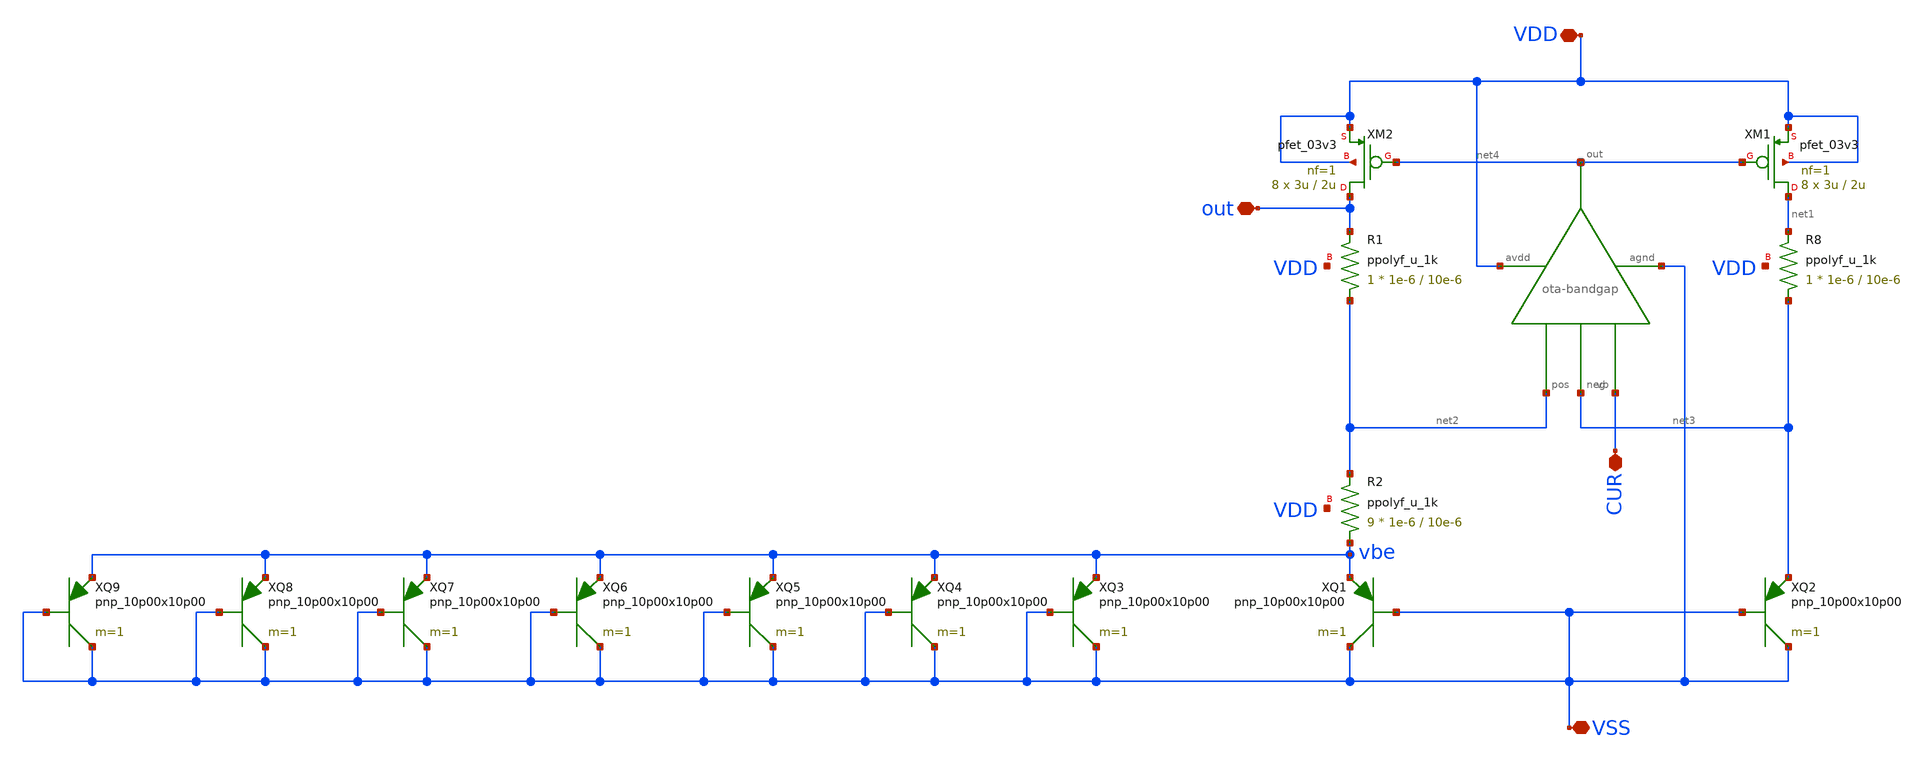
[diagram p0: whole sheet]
** sch_path: LDO/xschem/bandgap/bandgap.sch

.include $env(PDK_ROOT)/$env(PDK)/libs.tech/ngspice/design.ngspice
.lib $env(PDK_ROOT)/$env(PDK)/libs.tech/ngspice/sm141064.ngspice typical
.lib $env(PDK_ROOT)/$env(PDK)/libs.tech/ngspice/sm141064.ngspice mimcap_statistical
.lib $env(PDK_ROOT)/$env(PDK)/libs.tech/ngspice/sm141064.ngspice cap_mim
.lib $env(PDK_ROOT)/$env(PDK)/libs.tech/ngspice/sm141064.ngspice res_typical
.lib $env(PDK_ROOT)/$env(PDK)/libs.tech/ngspice/sm141064.ngspice bjt_typical
.lib $env(PDK_ROOT)/$env(PDK)/libs.tech/ngspice/sm141064.ngspice moscap_typical

**.subckt bandgap VDD VSS out CUR
*.iopin VDD
*.iopin VSS
*.iopin out
*.iopin CUR
XM1 net1 net4 VDD VDD pfet_03v3 L=2u W=3u nf=1 ad='int((nf+1)/2) * W/nf * 0.18u' as='int((nf+2)/2) * W/nf * 0.18u'
+ pd='2*int((nf+1)/2) * (W/nf + 0.18u)' ps='2*int((nf+2)/2) * (W/nf + 0.18u)' nrd='0.18u / W' nrs='0.18u / W'
+ sa=0 sb=0 sd=0 m=8
XM2 out net4 VDD VDD pfet_03v3 L=2u W=3u nf=1 ad='int((nf+1)/2) * W/nf * 0.18u' as='int((nf+2)/2) * W/nf * 0.18u'
+ pd='2*int((nf+1)/2) * (W/nf + 0.18u)' ps='2*int((nf+2)/2) * (W/nf + 0.18u)' nrd='0.18u / W' nrs='0.18u / W'
+ sa=0 sb=0 sd=0 m=8
X1 net4 VSS VDD net2 net3 CUR ota-bandgap
XQ1 VSS VSS vbe pnp_10p00x10p00 m=1
XQ2 VSS VSS net3 pnp_10p00x10p00 m=1
XQ3 VSS VSS vbe pnp_10p00x10p00 m=1
XQ4 VSS VSS vbe pnp_10p00x10p00 m=1
XQ5 VSS VSS vbe pnp_10p00x10p00 m=1
XQ6 VSS VSS vbe pnp_10p00x10p00 m=1
XQ7 VSS VSS vbe pnp_10p00x10p00 m=1
XQ8 VSS VSS vbe pnp_10p00x10p00 m=1
XQ9 VSS VSS vbe pnp_10p00x10p00 m=1
XR8 net3 net1 VDD ppolyf_u_1k r_width=1e-6 r_length=10e-6 m=1
XR1 net2 out VDD ppolyf_u_1k r_width=1e-6 r_length=10e-6 m=1
XR2 vbe net2 VDD ppolyf_u_1k r_width=1e-6 r_length=10e-6 m=9
**.ends
.end
